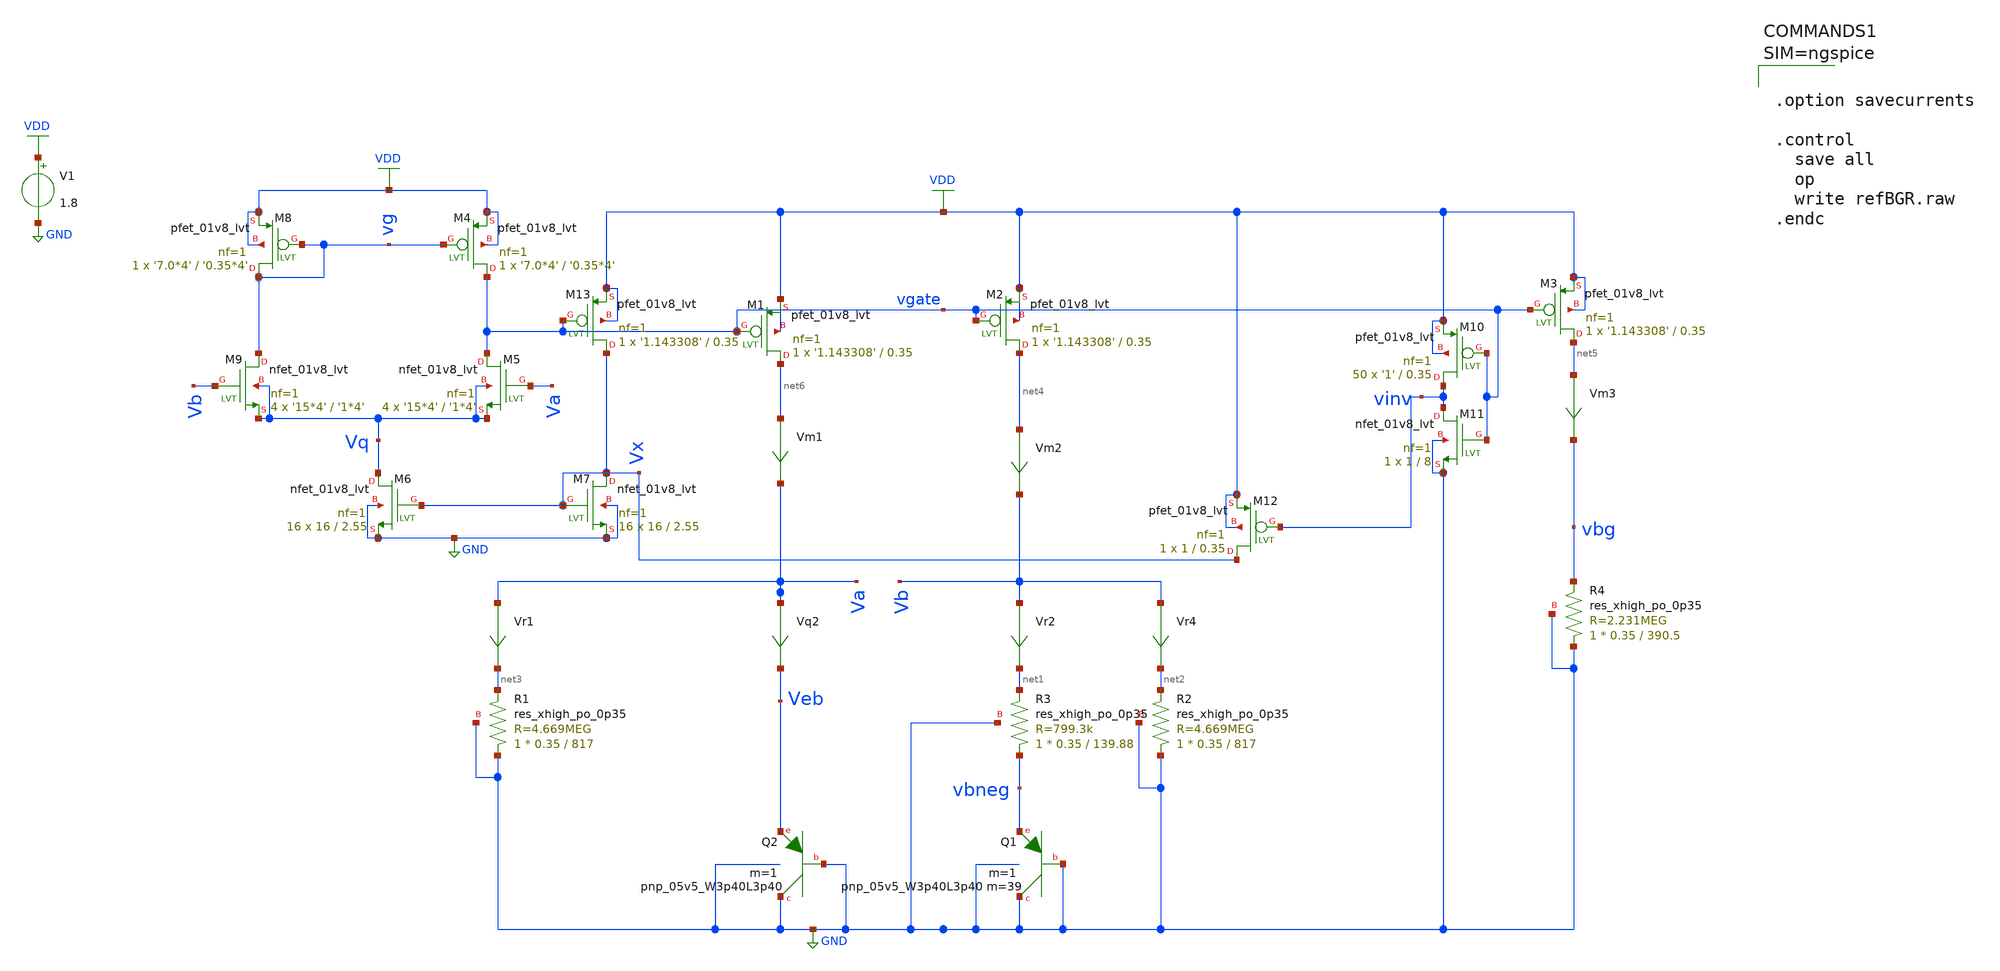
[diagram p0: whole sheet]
** sch_path: xschem/refBGR.sch
**.subckt refBGR
V1 VDD GND 1.8
XQ2 GND GND Veb sky130_fd_pr__pnp_05v5_W3p40L3p40 m=1
Vr4 Vb net2 0
.save i(vr4)
Vr2 Vb net1 0
.save i(vr2)
Vm1 net6 Va 0
.save i(vm1)
Vm2 net4 Vb 0
.save i(vm2)
Vm3 net5 vbg 0
.save i(vm3)
Vr1 Va net3 0
.save i(vr1)
Vq2 Va Veb 0
.save i(vq2)
XQ1 GND GND vbneg sky130_fd_pr__pnp_05v5_W3p40L3p40 m=39 m=1
XM4 vgate vg VDD VDD sky130_fd_pr__pfet_01v8_lvt L='0.35*4' W='7.0*4' nf=1 ad='int((nf+1)/2) * W/nf * 0.29'
+ as='int((nf+2)/2) * W/nf * 0.29' pd='2*int((nf+1)/2) * (W/nf + 0.29)' ps='2*int((nf+2)/2) * (W/nf + 0.29)'
+ nrd='0.29 / W' nrs='0.29 / W' sa=0 sb=0 sd=0 mult=1 m=1
XM5 vgate Va Vq Vq sky130_fd_pr__nfet_01v8_lvt L='1*4' W='15*4' nf=1 ad='int((nf+1)/2) * W/nf * 0.29'
+ as='int((nf+2)/2) * W/nf * 0.29' pd='2*int((nf+1)/2) * (W/nf + 0.29)' ps='2*int((nf+2)/2) * (W/nf + 0.29)'
+ nrd='0.29 / W' nrs='0.29 / W' sa=0 sb=0 sd=0 mult=4 m=4
XM6 Vq Vx GND GND sky130_fd_pr__nfet_01v8_lvt L=2.55 W=16 nf=1 ad='int((nf+1)/2) * W/nf * 0.29' as='int((nf+2)/2) * W/nf * 0.29'
+ pd='2*int((nf+1)/2) * (W/nf + 0.29)' ps='2*int((nf+2)/2) * (W/nf + 0.29)' nrd='0.29 / W' nrs='0.29 / W'
+ sa=0 sb=0 sd=0 mult=16 m=16
XM8 vg vg VDD VDD sky130_fd_pr__pfet_01v8_lvt L='0.35*4' W='7.0*4' nf=1 ad='int((nf+1)/2) * W/nf * 0.29'
+ as='int((nf+2)/2) * W/nf * 0.29' pd='2*int((nf+1)/2) * (W/nf + 0.29)' ps='2*int((nf+2)/2) * (W/nf + 0.29)'
+ nrd='0.29 / W' nrs='0.29 / W' sa=0 sb=0 sd=0 mult=1 m=1
XM9 vg Vb Vq Vq sky130_fd_pr__nfet_01v8_lvt L='1*4' W='15*4' nf=1 ad='int((nf+1)/2) * W/nf * 0.29' as='int((nf+2)/2) * W/nf * 0.29'
+ pd='2*int((nf+1)/2) * (W/nf + 0.29)' ps='2*int((nf+2)/2) * (W/nf + 0.29)' nrd='0.29 / W' nrs='0.29 / W'
+ sa=0 sb=0 sd=0 mult=4 m=4
XM10 vinv vgate VDD VDD sky130_fd_pr__pfet_01v8_lvt L=0.35 W='1' nf=1 ad='int((nf+1)/2) * W/nf * 0.29'
+ as='int((nf+2)/2) * W/nf * 0.29' pd='2*int((nf+1)/2) * (W/nf + 0.29)' ps='2*int((nf+2)/2) * (W/nf + 0.29)'
+ nrd='0.29 / W' nrs='0.29 / W' sa=0 sb=0 sd=0 mult=50 m=50
XM11 vinv vgate GND GND sky130_fd_pr__nfet_01v8_lvt L=8 W=1 nf=1 ad='int((nf+1)/2) * W/nf * 0.29' as='int((nf+2)/2) * W/nf * 0.29'
+ pd='2*int((nf+1)/2) * (W/nf + 0.29)' ps='2*int((nf+2)/2) * (W/nf + 0.29)' nrd='0.29 / W' nrs='0.29 / W'
+ sa=0 sb=0 sd=0 mult=1 m=1
XM12 Vx vinv VDD VDD sky130_fd_pr__pfet_01v8_lvt L=0.35 W=1 nf=1 ad='int((nf+1)/2) * W/nf * 0.29' as='int((nf+2)/2) * W/nf * 0.29'
+ pd='2*int((nf+1)/2) * (W/nf + 0.29)' ps='2*int((nf+2)/2) * (W/nf + 0.29)' nrd='0.29 / W' nrs='0.29 / W'
+ sa=0 sb=0 sd=0 mult=1 m=1
XM7 Vx Vx GND GND sky130_fd_pr__nfet_01v8_lvt L=2.55 W=16 nf=1 ad='int((nf+1)/2) * W/nf * 0.29' as='int((nf+2)/2) * W/nf * 0.29'
+ pd='2*int((nf+1)/2) * (W/nf + 0.29)' ps='2*int((nf+2)/2) * (W/nf + 0.29)' nrd='0.29 / W' nrs='0.29 / W'
+ sa=0 sb=0 sd=0 mult=16 m=16
XM13 Vx vgate VDD VDD sky130_fd_pr__pfet_01v8_lvt L=0.35 W='1.143308' nf=1 ad='int((nf+1)/2) * W/nf * 0.29'
+ as='int((nf+2)/2) * W/nf * 0.29' pd='2*int((nf+1)/2) * (W/nf + 0.29)' ps='2*int((nf+2)/2) * (W/nf + 0.29)'
+ nrd='0.29 / W' nrs='0.29 / W' sa=0 sb=0 sd=0 mult=1 m=1
XM1 net6 vgate VDD VDD sky130_fd_pr__pfet_01v8_lvt L=0.35 W='1.143308' nf=1 ad='int((nf+1)/2) * W/nf * 0.29'
+ as='int((nf+2)/2) * W/nf * 0.29' pd='2*int((nf+1)/2) * (W/nf + 0.29)' ps='2*int((nf+2)/2) * (W/nf + 0.29)'
+ nrd='0.29 / W' nrs='0.29 / W' sa=0 sb=0 sd=0 mult=1 m=1
XM2 net4 vgate VDD VDD sky130_fd_pr__pfet_01v8_lvt L=0.35 W='1.143308' nf=1 ad='int((nf+1)/2) * W/nf * 0.29'
+ as='int((nf+2)/2) * W/nf * 0.29' pd='2*int((nf+1)/2) * (W/nf + 0.29)' ps='2*int((nf+2)/2) * (W/nf + 0.29)'
+ nrd='0.29 / W' nrs='0.29 / W' sa=0 sb=0 sd=0 mult=1 m=1
XM3 net5 vgate VDD VDD sky130_fd_pr__pfet_01v8_lvt L=0.35 W='1.143308' nf=1 ad='int((nf+1)/2) * W/nf * 0.29'
+ as='int((nf+2)/2) * W/nf * 0.29' pd='2*int((nf+1)/2) * (W/nf + 0.29)' ps='2*int((nf+2)/2) * (W/nf + 0.29)'
+ nrd='0.29 / W' nrs='0.29 / W' sa=0 sb=0 sd=0 mult=1 m=1
XR1 GND net3 GND sky130_fd_pr__res_xhigh_po_0p35 L=817 mult=1 m=1
XR2 GND net2 GND sky130_fd_pr__res_xhigh_po_0p35 L=817 mult=1 m=1
XR3 vbneg net1 GND sky130_fd_pr__res_xhigh_po_0p35 L=139.88 mult=1 m=1
XR4 GND vbg GND sky130_fd_pr__res_xhigh_po_0p35 L=390.5 mult=1 m=1
**** begin user architecture code



.option savecurrents

.control
  save all
  op
  write refBGR.raw
.endc




** opencircuitdesign pdks install
.lib $::SKYWATER_MODELS/sky130.lib.spice tt


**** end user architecture code
**.ends
.GLOBAL VDD
.GLOBAL GND
.end
